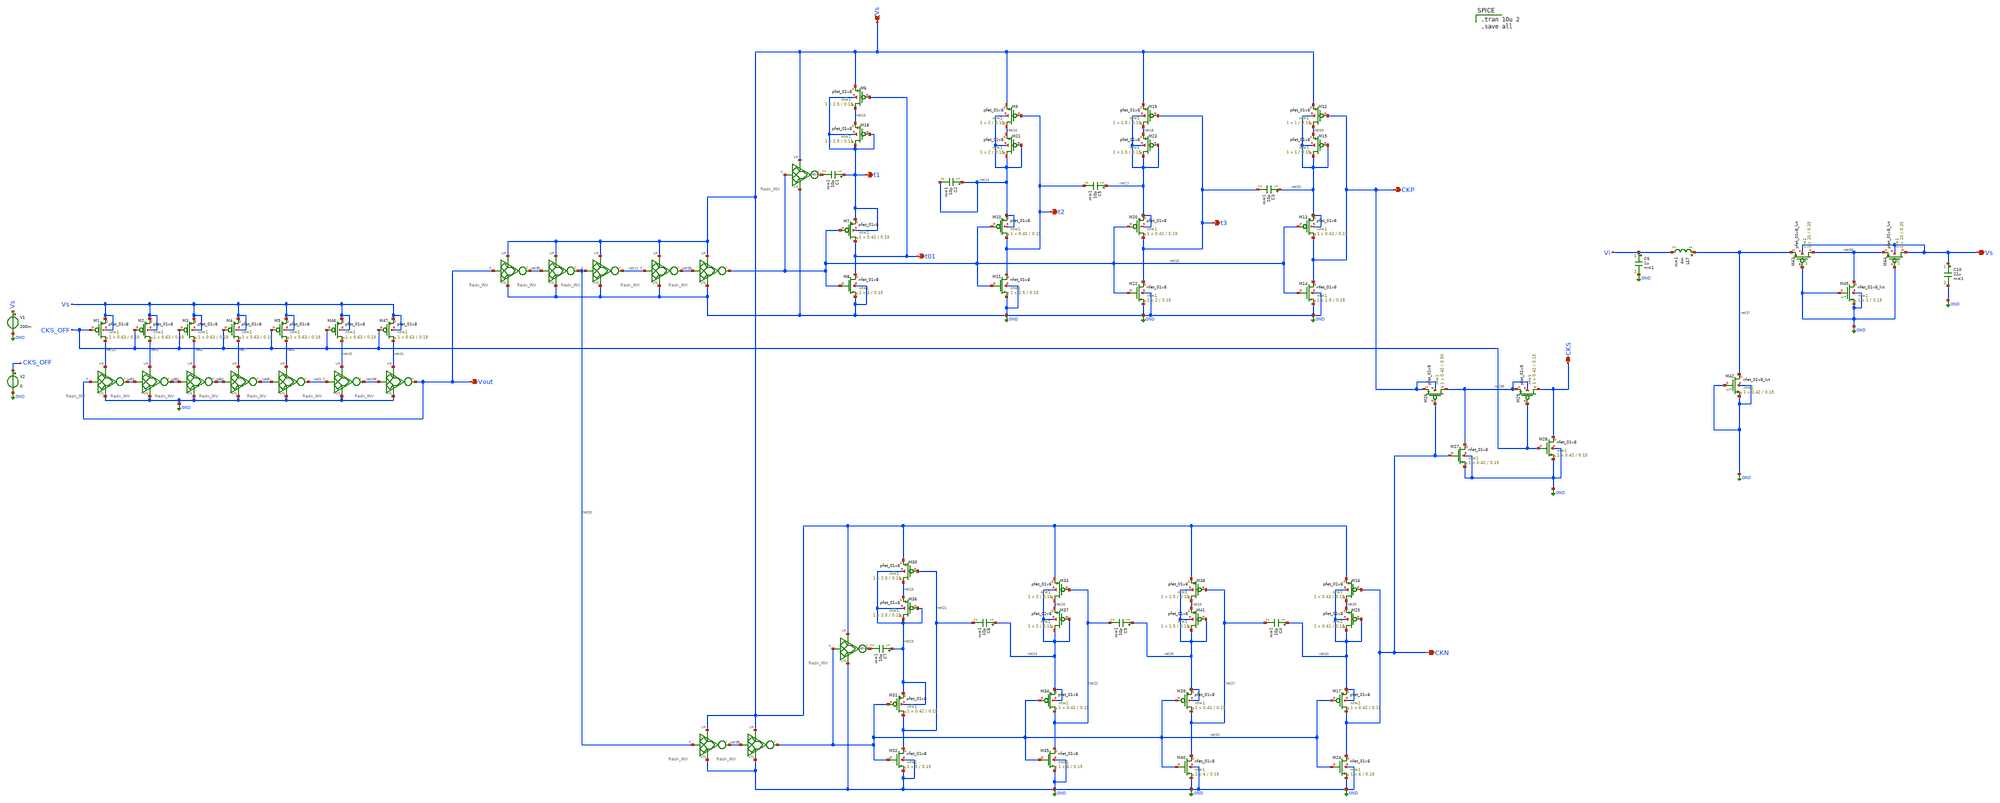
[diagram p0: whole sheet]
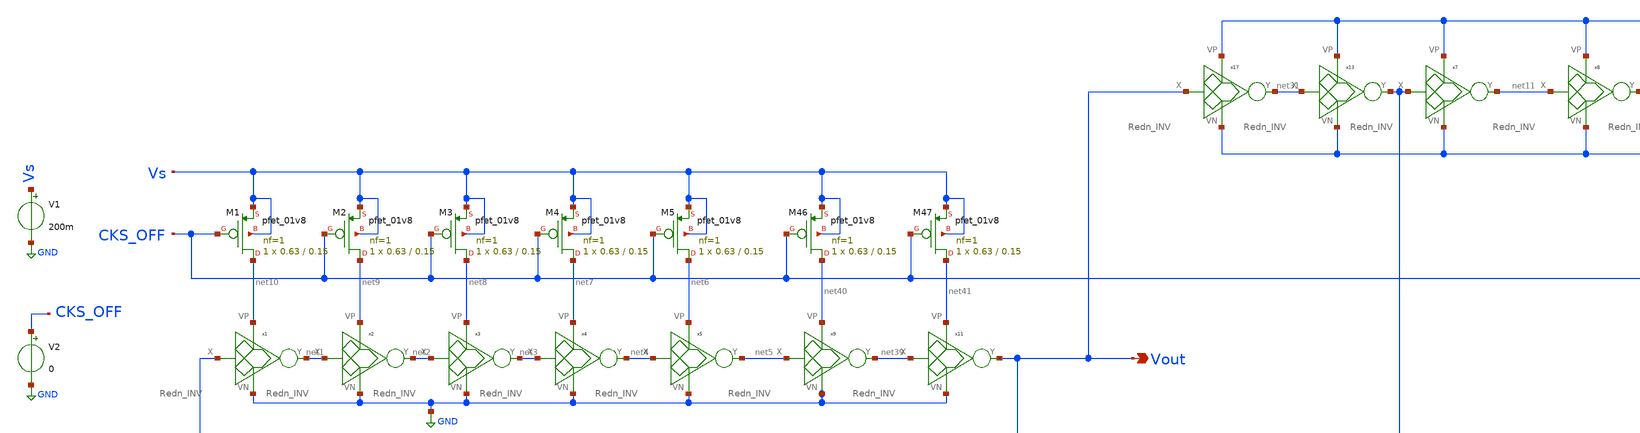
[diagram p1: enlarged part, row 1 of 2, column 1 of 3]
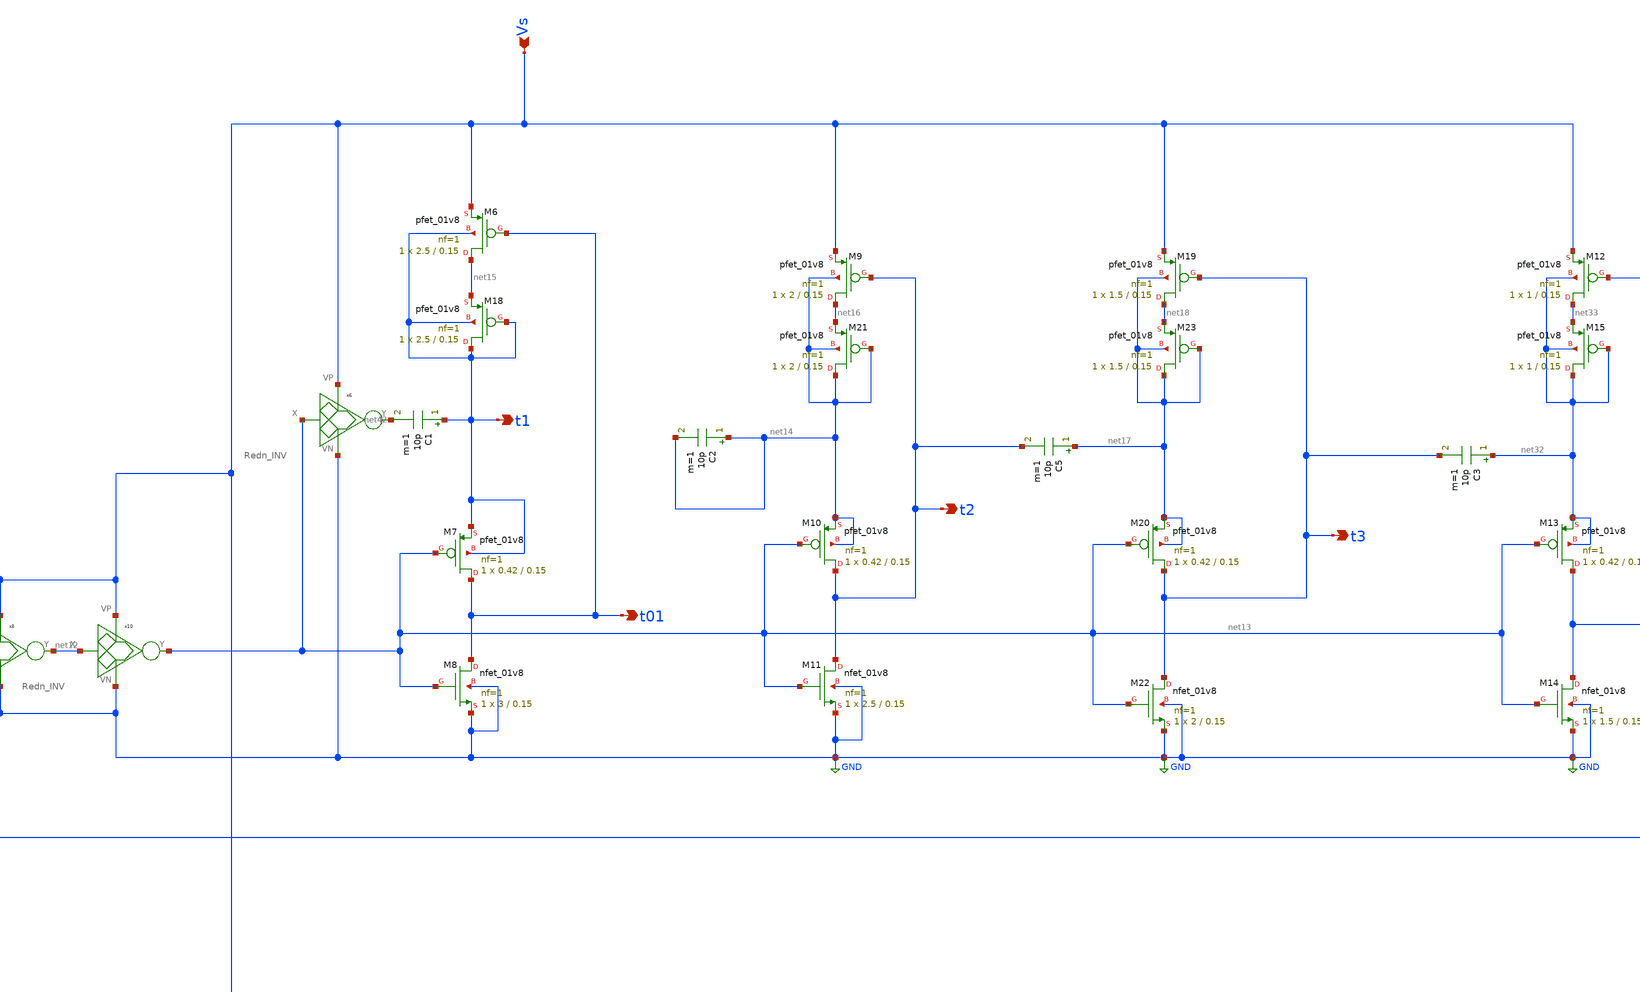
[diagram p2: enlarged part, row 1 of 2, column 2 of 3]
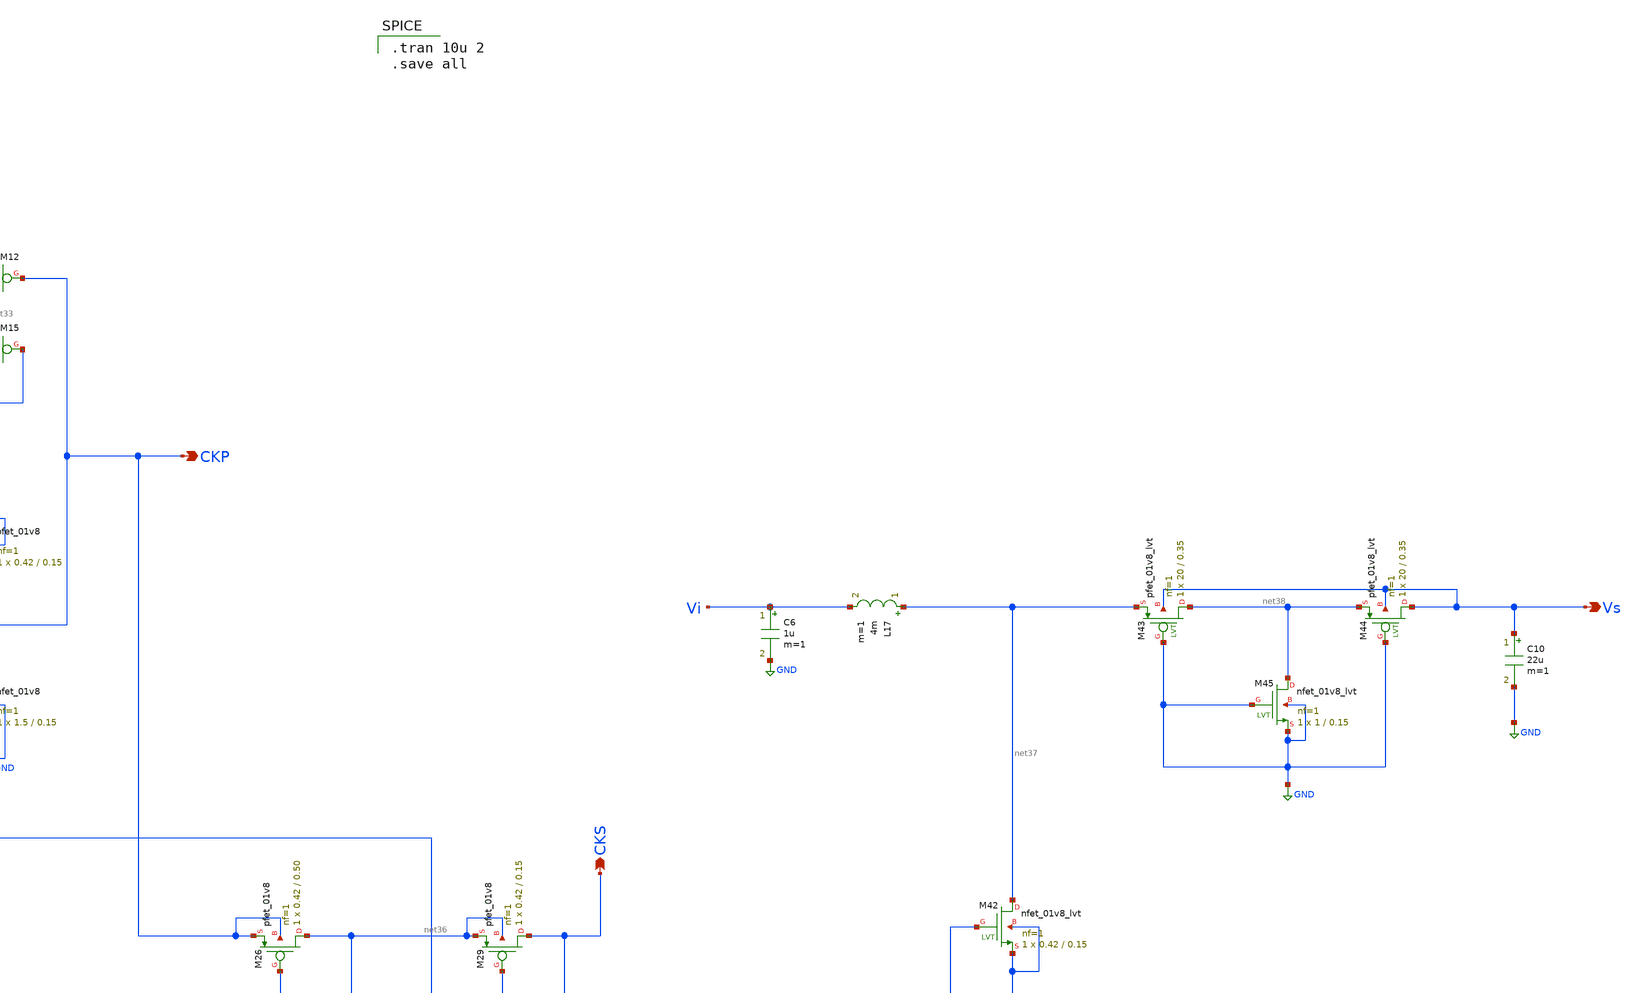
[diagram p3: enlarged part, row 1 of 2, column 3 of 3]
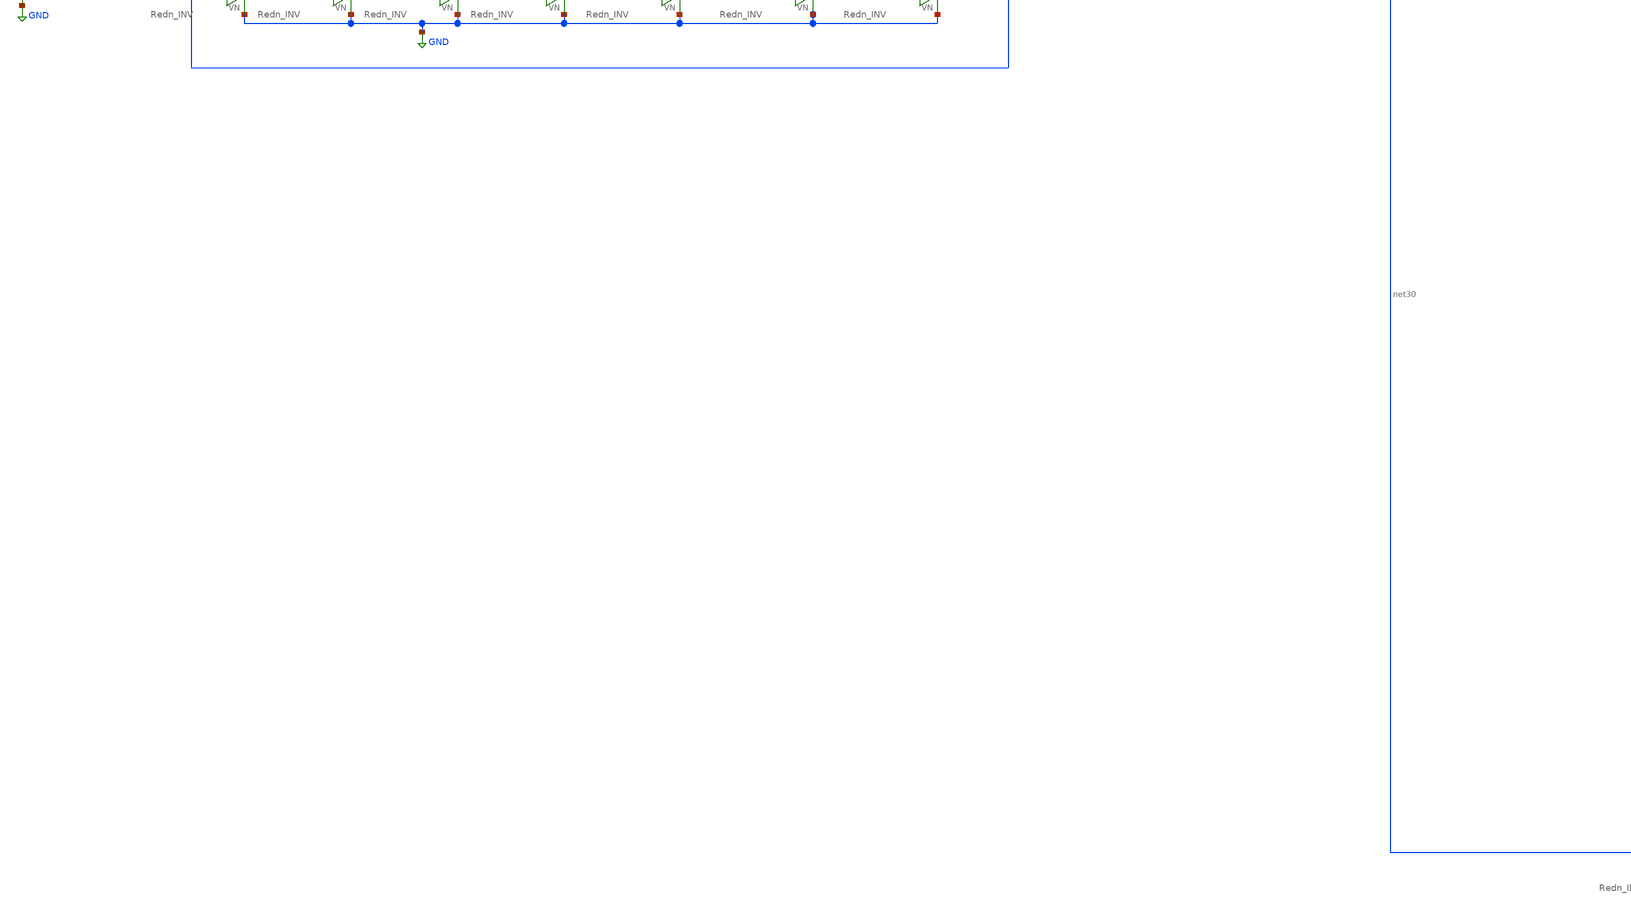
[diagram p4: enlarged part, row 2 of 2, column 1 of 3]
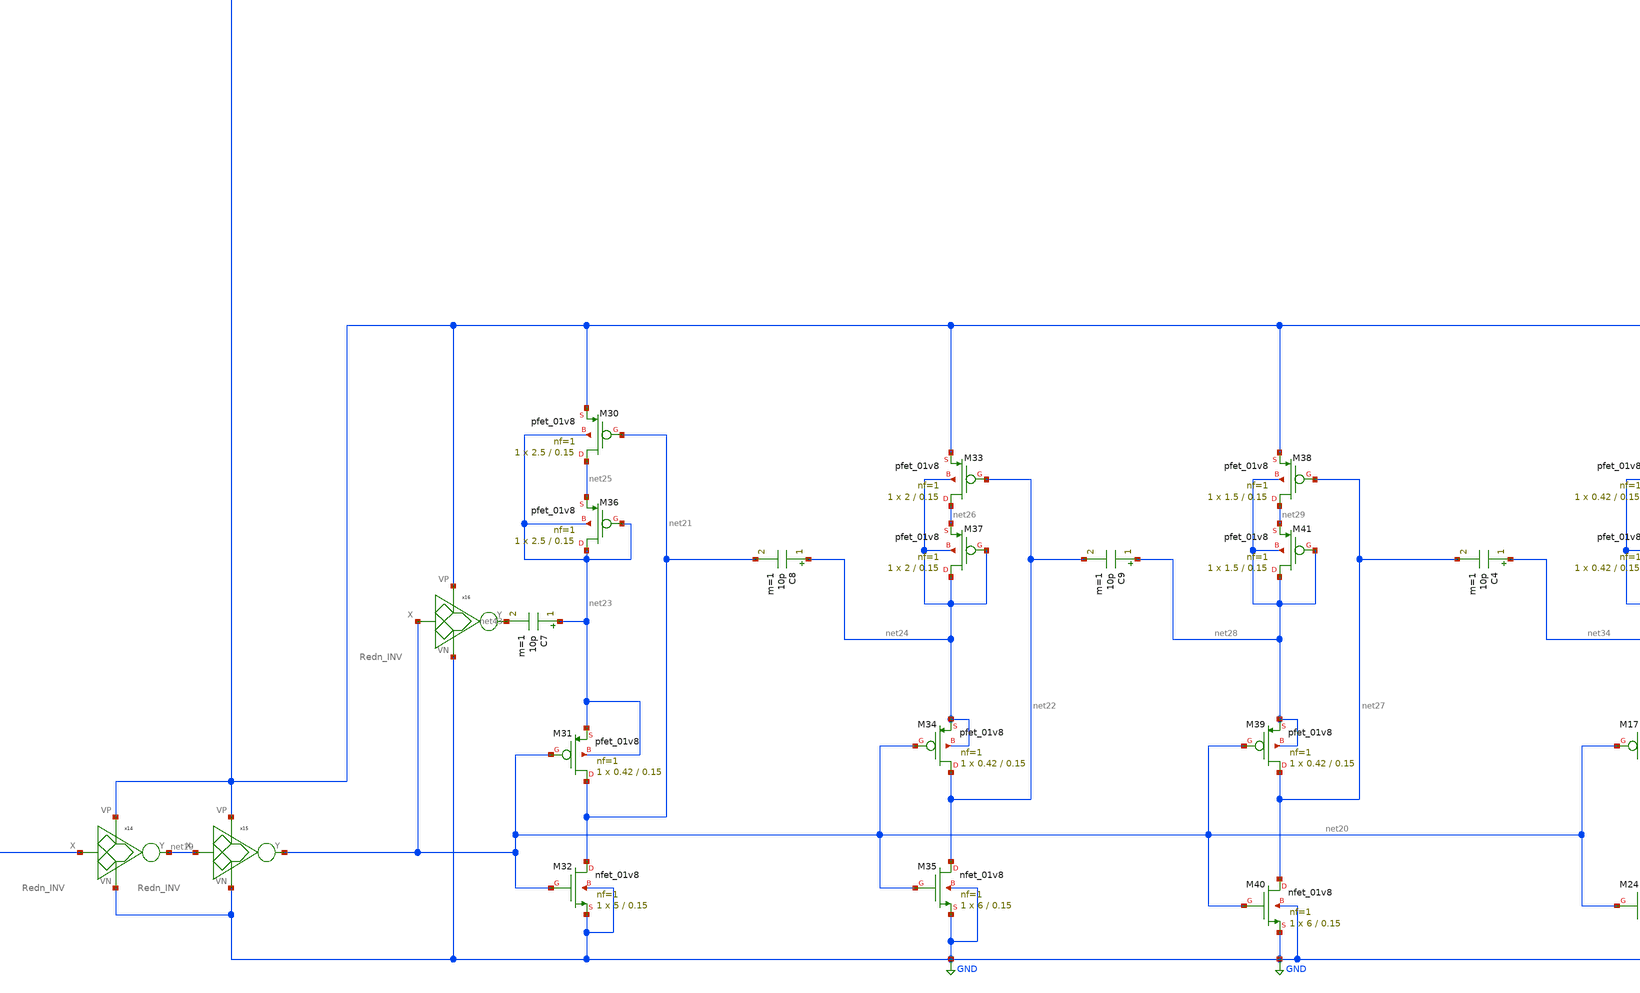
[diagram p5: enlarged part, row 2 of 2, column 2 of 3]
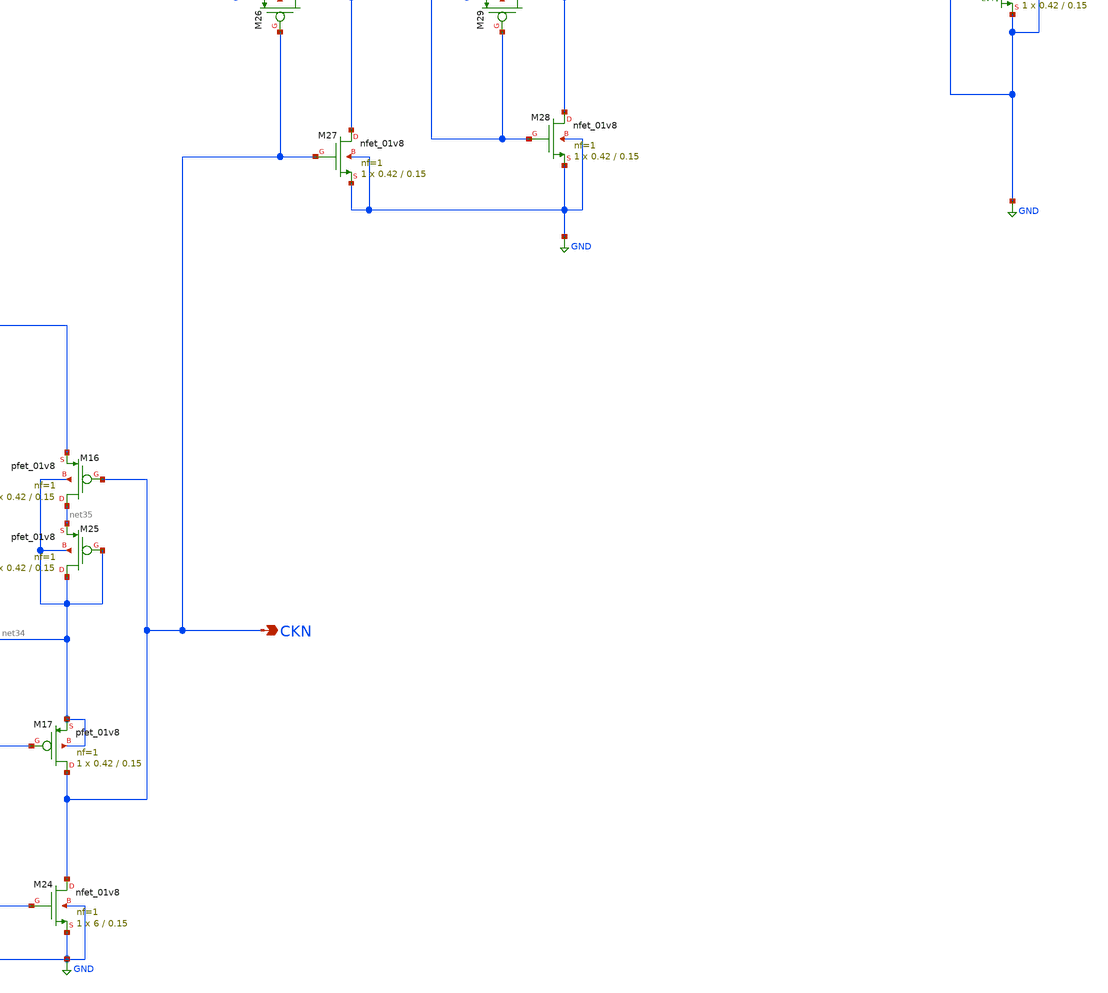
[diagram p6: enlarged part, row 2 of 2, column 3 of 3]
** sch_path: Blocks/Startup Converter/test_2.sch
**.subckt test_2 Vout Vs t1 t2 CKP CKN CKS Vs t3 t01
*.opin Vout
*.ipin Vs
*.opin t1
*.opin t2
*.opin CKP
*.opin CKN
*.opin CKS
*.opin Vs
*.opin t3
*.opin t01
V1 Vs GND 200m
XM1 net10 CKS_OFF Vs Vs sky130_fd_pr__pfet_01v8 L=0.15 W=0.63 nf=1 ad='int((nf+1)/2) * W/nf * 0.29' as='int((nf+2)/2) * W/nf * 0.29'
+ pd='2*int((nf+1)/2) * (W/nf + 0.29)' ps='2*int((nf+2)/2) * (W/nf + 0.29)' nrd='0.29 / W' nrs='0.29 / W'
+ sa=0 sb=0 sd=0 mult=1 m=1
XM2 net9 CKS_OFF Vs Vs sky130_fd_pr__pfet_01v8 L=0.15 W=0.63 nf=1 ad='int((nf+1)/2) * W/nf * 0.29' as='int((nf+2)/2) * W/nf * 0.29'
+ pd='2*int((nf+1)/2) * (W/nf + 0.29)' ps='2*int((nf+2)/2) * (W/nf + 0.29)' nrd='0.29 / W' nrs='0.29 / W'
+ sa=0 sb=0 sd=0 mult=1 m=1
XM3 net8 CKS_OFF Vs Vs sky130_fd_pr__pfet_01v8 L=0.15 W=0.63 nf=1 ad='int((nf+1)/2) * W/nf * 0.29' as='int((nf+2)/2) * W/nf * 0.29'
+ pd='2*int((nf+1)/2) * (W/nf + 0.29)' ps='2*int((nf+2)/2) * (W/nf + 0.29)' nrd='0.29 / W' nrs='0.29 / W'
+ sa=0 sb=0 sd=0 mult=1 m=1
XM4 net7 CKS_OFF Vs Vs sky130_fd_pr__pfet_01v8 L=0.15 W=0.63 nf=1 ad='int((nf+1)/2) * W/nf * 0.29' as='int((nf+2)/2) * W/nf * 0.29'
+ pd='2*int((nf+1)/2) * (W/nf + 0.29)' ps='2*int((nf+2)/2) * (W/nf + 0.29)' nrd='0.29 / W' nrs='0.29 / W'
+ sa=0 sb=0 sd=0 mult=1 m=1
XM5 net6 CKS_OFF Vs Vs sky130_fd_pr__pfet_01v8 L=0.15 W=0.63 nf=1 ad='int((nf+1)/2) * W/nf * 0.29' as='int((nf+2)/2) * W/nf * 0.29'
+ pd='2*int((nf+1)/2) * (W/nf + 0.29)' ps='2*int((nf+2)/2) * (W/nf + 0.29)' nrd='0.29 / W' nrs='0.29 / W'
+ sa=0 sb=0 sd=0 mult=1 m=1
V2 CKS_OFF GND 0
x1 Vout net1 net10 GND Redn_INV
x2 net1 net2 net9 GND Redn_INV
x3 net2 net3 net8 GND Redn_INV
x4 net3 net4 net7 GND Redn_INV
x5 net4 net5 net6 GND Redn_INV
C1 t1 net42 10p m=1
XM6 net15 t01 Vs t1 sky130_fd_pr__pfet_01v8 L=0.15 W=2.5 nf=1 ad='int((nf+1)/2) * W/nf * 0.29' as='int((nf+2)/2) * W/nf * 0.29'
+ pd='2*int((nf+1)/2) * (W/nf + 0.29)' ps='2*int((nf+2)/2) * (W/nf + 0.29)' nrd='0.29 / W' nrs='0.29 / W'
+ sa=0 sb=0 sd=0 mult=1 m=1
XM7 t01 net13 t1 t1 sky130_fd_pr__pfet_01v8 L=0.15 W=0.42 nf=1 ad='int((nf+1)/2) * W/nf * 0.29' as='int((nf+2)/2) * W/nf * 0.29'
+ pd='2*int((nf+1)/2) * (W/nf + 0.29)' ps='2*int((nf+2)/2) * (W/nf + 0.29)' nrd='0.29 / W' nrs='0.29 / W'
+ sa=0 sb=0 sd=0 mult=1 m=1
XM8 t01 net13 GND GND sky130_fd_pr__nfet_01v8 L=0.15 W=3 nf=1 ad='int((nf+1)/2) * W/nf * 0.29' as='int((nf+2)/2) * W/nf * 0.29'
+ pd='2*int((nf+1)/2) * (W/nf + 0.29)' ps='2*int((nf+2)/2) * (W/nf + 0.29)' nrd='0.29 / W' nrs='0.29 / W'
+ sa=0 sb=0 sd=0 mult=1 m=1
XM9 net16 t2 Vs net14 sky130_fd_pr__pfet_01v8 L=0.15 W=2 nf=1 ad='int((nf+1)/2) * W/nf * 0.29' as='int((nf+2)/2) * W/nf * 0.29'
+ pd='2*int((nf+1)/2) * (W/nf + 0.29)' ps='2*int((nf+2)/2) * (W/nf + 0.29)' nrd='0.29 / W' nrs='0.29 / W'
+ sa=0 sb=0 sd=0 mult=1 m=1
XM10 t2 net13 net14 net14 sky130_fd_pr__pfet_01v8 L=0.15 W=0.42 nf=1 ad='int((nf+1)/2) * W/nf * 0.29'
+ as='int((nf+2)/2) * W/nf * 0.29' pd='2*int((nf+1)/2) * (W/nf + 0.29)' ps='2*int((nf+2)/2) * (W/nf + 0.29)'
+ nrd='0.29 / W' nrs='0.29 / W' sa=0 sb=0 sd=0 mult=1 m=1
XM11 t2 net13 GND GND sky130_fd_pr__nfet_01v8 L=0.15 W=2.5 nf=1 ad='int((nf+1)/2) * W/nf * 0.29' as='int((nf+2)/2) * W/nf * 0.29'
+ pd='2*int((nf+1)/2) * (W/nf + 0.29)' ps='2*int((nf+2)/2) * (W/nf + 0.29)' nrd='0.29 / W' nrs='0.29 / W'
+ sa=0 sb=0 sd=0 mult=1 m=1
XM18 t1 t1 net15 t1 sky130_fd_pr__pfet_01v8 L=0.15 W=2.5 nf=1 ad='int((nf+1)/2) * W/nf * 0.29' as='int((nf+2)/2) * W/nf * 0.29'
+ pd='2*int((nf+1)/2) * (W/nf + 0.29)' ps='2*int((nf+2)/2) * (W/nf + 0.29)' nrd='0.29 / W' nrs='0.29 / W'
+ sa=0 sb=0 sd=0 mult=1 m=1
XM21 net14 net14 net16 net14 sky130_fd_pr__pfet_01v8 L=0.15 W=2 nf=1 ad='int((nf+1)/2) * W/nf * 0.29'
+ as='int((nf+2)/2) * W/nf * 0.29' pd='2*int((nf+1)/2) * (W/nf + 0.29)' ps='2*int((nf+2)/2) * (W/nf + 0.29)'
+ nrd='0.29 / W' nrs='0.29 / W' sa=0 sb=0 sd=0 mult=1 m=1
C2 net14 net14 10p m=1
x7 net30 net11 Vs GND Redn_INV
x8 net11 net12 Vs GND Redn_INV
x10 net12 net13 Vs GND Redn_INV
x6 net13 net42 Vs GND Redn_INV
XM19 net18 t3 Vs net17 sky130_fd_pr__pfet_01v8 L=0.15 W=1.5 nf=1 ad='int((nf+1)/2) * W/nf * 0.29' as='int((nf+2)/2) * W/nf * 0.29'
+ pd='2*int((nf+1)/2) * (W/nf + 0.29)' ps='2*int((nf+2)/2) * (W/nf + 0.29)' nrd='0.29 / W' nrs='0.29 / W'
+ sa=0 sb=0 sd=0 mult=1 m=1
XM20 t3 net13 net17 net17 sky130_fd_pr__pfet_01v8 L=0.15 W=0.42 nf=1 ad='int((nf+1)/2) * W/nf * 0.29'
+ as='int((nf+2)/2) * W/nf * 0.29' pd='2*int((nf+1)/2) * (W/nf + 0.29)' ps='2*int((nf+2)/2) * (W/nf + 0.29)'
+ nrd='0.29 / W' nrs='0.29 / W' sa=0 sb=0 sd=0 mult=1 m=1
XM22 t3 net13 GND GND sky130_fd_pr__nfet_01v8 L=0.15 W=2 nf=1 ad='int((nf+1)/2) * W/nf * 0.29' as='int((nf+2)/2) * W/nf * 0.29'
+ pd='2*int((nf+1)/2) * (W/nf + 0.29)' ps='2*int((nf+2)/2) * (W/nf + 0.29)' nrd='0.29 / W' nrs='0.29 / W'
+ sa=0 sb=0 sd=0 mult=1 m=1
XM23 net17 net17 net18 net17 sky130_fd_pr__pfet_01v8 L=0.15 W=1.5 nf=1 ad='int((nf+1)/2) * W/nf * 0.29'
+ as='int((nf+2)/2) * W/nf * 0.29' pd='2*int((nf+1)/2) * (W/nf + 0.29)' ps='2*int((nf+2)/2) * (W/nf + 0.29)'
+ nrd='0.29 / W' nrs='0.29 / W' sa=0 sb=0 sd=0 mult=1 m=1
C5 net17 t2 10p m=1
C7 net23 net43 10p m=1
XM30 net25 net21 Vs net23 sky130_fd_pr__pfet_01v8 L=0.15 W=2.5 nf=1 ad='int((nf+1)/2) * W/nf * 0.29'
+ as='int((nf+2)/2) * W/nf * 0.29' pd='2*int((nf+1)/2) * (W/nf + 0.29)' ps='2*int((nf+2)/2) * (W/nf + 0.29)'
+ nrd='0.29 / W' nrs='0.29 / W' sa=0 sb=0 sd=0 mult=1 m=1
XM31 net21 net20 net23 net23 sky130_fd_pr__pfet_01v8 L=0.15 W=0.42 nf=1 ad='int((nf+1)/2) * W/nf * 0.29'
+ as='int((nf+2)/2) * W/nf * 0.29' pd='2*int((nf+1)/2) * (W/nf + 0.29)' ps='2*int((nf+2)/2) * (W/nf + 0.29)'
+ nrd='0.29 / W' nrs='0.29 / W' sa=0 sb=0 sd=0 mult=1 m=1
XM32 net21 net20 GND GND sky130_fd_pr__nfet_01v8 L=0.15 W=5 nf=1 ad='int((nf+1)/2) * W/nf * 0.29' as='int((nf+2)/2) * W/nf * 0.29'
+ pd='2*int((nf+1)/2) * (W/nf + 0.29)' ps='2*int((nf+2)/2) * (W/nf + 0.29)' nrd='0.29 / W' nrs='0.29 / W'
+ sa=0 sb=0 sd=0 mult=1 m=1
XM33 net26 net22 Vs net24 sky130_fd_pr__pfet_01v8 L=0.15 W=2 nf=1 ad='int((nf+1)/2) * W/nf * 0.29' as='int((nf+2)/2) * W/nf * 0.29'
+ pd='2*int((nf+1)/2) * (W/nf + 0.29)' ps='2*int((nf+2)/2) * (W/nf + 0.29)' nrd='0.29 / W' nrs='0.29 / W'
+ sa=0 sb=0 sd=0 mult=1 m=1
XM34 net22 net20 net24 net24 sky130_fd_pr__pfet_01v8 L=0.15 W=0.42 nf=1 ad='int((nf+1)/2) * W/nf * 0.29'
+ as='int((nf+2)/2) * W/nf * 0.29' pd='2*int((nf+1)/2) * (W/nf + 0.29)' ps='2*int((nf+2)/2) * (W/nf + 0.29)'
+ nrd='0.29 / W' nrs='0.29 / W' sa=0 sb=0 sd=0 mult=1 m=1
XM35 net22 net20 GND GND sky130_fd_pr__nfet_01v8 L=0.15 W=6 nf=1 ad='int((nf+1)/2) * W/nf * 0.29' as='int((nf+2)/2) * W/nf * 0.29'
+ pd='2*int((nf+1)/2) * (W/nf + 0.29)' ps='2*int((nf+2)/2) * (W/nf + 0.29)' nrd='0.29 / W' nrs='0.29 / W'
+ sa=0 sb=0 sd=0 mult=1 m=1
XM36 net23 net23 net25 net23 sky130_fd_pr__pfet_01v8 L=0.15 W=2.5 nf=1 ad='int((nf+1)/2) * W/nf * 0.29'
+ as='int((nf+2)/2) * W/nf * 0.29' pd='2*int((nf+1)/2) * (W/nf + 0.29)' ps='2*int((nf+2)/2) * (W/nf + 0.29)'
+ nrd='0.29 / W' nrs='0.29 / W' sa=0 sb=0 sd=0 mult=1 m=1
XM37 net24 net24 net26 net24 sky130_fd_pr__pfet_01v8 L=0.15 W=2 nf=1 ad='int((nf+1)/2) * W/nf * 0.29'
+ as='int((nf+2)/2) * W/nf * 0.29' pd='2*int((nf+1)/2) * (W/nf + 0.29)' ps='2*int((nf+2)/2) * (W/nf + 0.29)'
+ nrd='0.29 / W' nrs='0.29 / W' sa=0 sb=0 sd=0 mult=1 m=1
C8 net24 net21 10p m=1
x14 net30 net19 Vs GND Redn_INV
x15 net19 net20 Vs GND Redn_INV
x16 net20 net43 Vs GND Redn_INV
XM38 net29 net27 Vs net28 sky130_fd_pr__pfet_01v8 L=0.15 W=1.5 nf=1 ad='int((nf+1)/2) * W/nf * 0.29'
+ as='int((nf+2)/2) * W/nf * 0.29' pd='2*int((nf+1)/2) * (W/nf + 0.29)' ps='2*int((nf+2)/2) * (W/nf + 0.29)'
+ nrd='0.29 / W' nrs='0.29 / W' sa=0 sb=0 sd=0 mult=1 m=1
XM39 net27 net20 net28 net28 sky130_fd_pr__pfet_01v8 L=0.15 W=0.42 nf=1 ad='int((nf+1)/2) * W/nf * 0.29'
+ as='int((nf+2)/2) * W/nf * 0.29' pd='2*int((nf+1)/2) * (W/nf + 0.29)' ps='2*int((nf+2)/2) * (W/nf + 0.29)'
+ nrd='0.29 / W' nrs='0.29 / W' sa=0 sb=0 sd=0 mult=1 m=1
XM40 net27 net20 GND GND sky130_fd_pr__nfet_01v8 L=0.15 W=6 nf=1 ad='int((nf+1)/2) * W/nf * 0.29' as='int((nf+2)/2) * W/nf * 0.29'
+ pd='2*int((nf+1)/2) * (W/nf + 0.29)' ps='2*int((nf+2)/2) * (W/nf + 0.29)' nrd='0.29 / W' nrs='0.29 / W'
+ sa=0 sb=0 sd=0 mult=1 m=1
XM41 net28 net28 net29 net28 sky130_fd_pr__pfet_01v8 L=0.15 W=1.5 nf=1 ad='int((nf+1)/2) * W/nf * 0.29'
+ as='int((nf+2)/2) * W/nf * 0.29' pd='2*int((nf+1)/2) * (W/nf + 0.29)' ps='2*int((nf+2)/2) * (W/nf + 0.29)'
+ nrd='0.29 / W' nrs='0.29 / W' sa=0 sb=0 sd=0 mult=1 m=1
C9 net28 net22 10p m=1
x13 net31 net30 Vs GND Redn_INV
x17 Vout net31 Vs GND Redn_INV
XM12 net33 CKP Vs net32 sky130_fd_pr__pfet_01v8 L=0.15 W=1 nf=1 ad='int((nf+1)/2) * W/nf * 0.29' as='int((nf+2)/2) * W/nf * 0.29'
+ pd='2*int((nf+1)/2) * (W/nf + 0.29)' ps='2*int((nf+2)/2) * (W/nf + 0.29)' nrd='0.29 / W' nrs='0.29 / W'
+ sa=0 sb=0 sd=0 mult=1 m=1
XM13 CKP net13 net32 net32 sky130_fd_pr__pfet_01v8 L=0.15 W=0.42 nf=1 ad='int((nf+1)/2) * W/nf * 0.29'
+ as='int((nf+2)/2) * W/nf * 0.29' pd='2*int((nf+1)/2) * (W/nf + 0.29)' ps='2*int((nf+2)/2) * (W/nf + 0.29)'
+ nrd='0.29 / W' nrs='0.29 / W' sa=0 sb=0 sd=0 mult=1 m=1
XM14 CKP net13 GND GND sky130_fd_pr__nfet_01v8 L=0.15 W=1.5 nf=1 ad='int((nf+1)/2) * W/nf * 0.29' as='int((nf+2)/2) * W/nf * 0.29'
+ pd='2*int((nf+1)/2) * (W/nf + 0.29)' ps='2*int((nf+2)/2) * (W/nf + 0.29)' nrd='0.29 / W' nrs='0.29 / W'
+ sa=0 sb=0 sd=0 mult=1 m=1
XM15 net32 net32 net33 net32 sky130_fd_pr__pfet_01v8 L=0.15 W=1 nf=1 ad='int((nf+1)/2) * W/nf * 0.29'
+ as='int((nf+2)/2) * W/nf * 0.29' pd='2*int((nf+1)/2) * (W/nf + 0.29)' ps='2*int((nf+2)/2) * (W/nf + 0.29)'
+ nrd='0.29 / W' nrs='0.29 / W' sa=0 sb=0 sd=0 mult=1 m=1
C3 net32 t3 10p m=1
XM16 net35 CKN Vs net34 sky130_fd_pr__pfet_01v8 L=0.15 W=0.42 nf=1 ad='int((nf+1)/2) * W/nf * 0.29' as='int((nf+2)/2) * W/nf * 0.29'
+ pd='2*int((nf+1)/2) * (W/nf + 0.29)' ps='2*int((nf+2)/2) * (W/nf + 0.29)' nrd='0.29 / W' nrs='0.29 / W'
+ sa=0 sb=0 sd=0 mult=1 m=1
XM17 CKN net20 net34 net34 sky130_fd_pr__pfet_01v8 L=0.15 W=0.42 nf=1 ad='int((nf+1)/2) * W/nf * 0.29'
+ as='int((nf+2)/2) * W/nf * 0.29' pd='2*int((nf+1)/2) * (W/nf + 0.29)' ps='2*int((nf+2)/2) * (W/nf + 0.29)'
+ nrd='0.29 / W' nrs='0.29 / W' sa=0 sb=0 sd=0 mult=1 m=1
XM24 CKN net20 GND GND sky130_fd_pr__nfet_01v8 L=0.15 W=6 nf=1 ad='int((nf+1)/2) * W/nf * 0.29' as='int((nf+2)/2) * W/nf * 0.29'
+ pd='2*int((nf+1)/2) * (W/nf + 0.29)' ps='2*int((nf+2)/2) * (W/nf + 0.29)' nrd='0.29 / W' nrs='0.29 / W'
+ sa=0 sb=0 sd=0 mult=1 m=1
XM25 net34 net34 net35 net34 sky130_fd_pr__pfet_01v8 L=0.15 W=0.42 nf=1 ad='int((nf+1)/2) * W/nf * 0.29'
+ as='int((nf+2)/2) * W/nf * 0.29' pd='2*int((nf+1)/2) * (W/nf + 0.29)' ps='2*int((nf+2)/2) * (W/nf + 0.29)'
+ nrd='0.29 / W' nrs='0.29 / W' sa=0 sb=0 sd=0 mult=1 m=1
C4 net34 net27 10p m=1
XM26 net36 CKN CKP CKP sky130_fd_pr__pfet_01v8 L=0.50 W=0.42 nf=1 ad='int((nf+1)/2) * W/nf * 0.29' as='int((nf+2)/2) * W/nf * 0.29'
+ pd='2*int((nf+1)/2) * (W/nf + 0.29)' ps='2*int((nf+2)/2) * (W/nf + 0.29)' nrd='0.29 / W' nrs='0.29 / W'
+ sa=0 sb=0 sd=0 mult=1 m=1
XM27 net36 CKN GND GND sky130_fd_pr__nfet_01v8 L=0.15 W=0.42 nf=1 ad='int((nf+1)/2) * W/nf * 0.29' as='int((nf+2)/2) * W/nf * 0.29'
+ pd='2*int((nf+1)/2) * (W/nf + 0.29)' ps='2*int((nf+2)/2) * (W/nf + 0.29)' nrd='0.29 / W' nrs='0.29 / W'
+ sa=0 sb=0 sd=0 mult=1 m=1
XM28 CKS CKS_OFF GND GND sky130_fd_pr__nfet_01v8 L=0.15 W=0.42 nf=1 ad='int((nf+1)/2) * W/nf * 0.29'
+ as='int((nf+2)/2) * W/nf * 0.29' pd='2*int((nf+1)/2) * (W/nf + 0.29)' ps='2*int((nf+2)/2) * (W/nf + 0.29)'
+ nrd='0.29 / W' nrs='0.29 / W' sa=0 sb=0 sd=0 mult=1 m=1
XM29 CKS CKS_OFF net36 net36 sky130_fd_pr__pfet_01v8 L=0.15 W=0.42 nf=1 ad='int((nf+1)/2) * W/nf * 0.29'
+ as='int((nf+2)/2) * W/nf * 0.29' pd='2*int((nf+1)/2) * (W/nf + 0.29)' ps='2*int((nf+2)/2) * (W/nf + 0.29)'
+ nrd='0.29 / W' nrs='0.29 / W' sa=0 sb=0 sd=0 mult=1 m=1
C6 Vi GND 1u m=1
L17 net37 Vi 4m m=1
C10 Vs GND 22u m=1
XM42 net37 GND GND GND sky130_fd_pr__nfet_01v8_lvt L=0.15 W=0.42 nf=1 ad='int((nf+1)/2) * W/nf * 0.29'
+ as='int((nf+2)/2) * W/nf * 0.29' pd='2*int((nf+1)/2) * (W/nf + 0.29)' ps='2*int((nf+2)/2) * (W/nf + 0.29)'
+ nrd='0.29 / W' nrs='0.29 / W' sa=0 sb=0 sd=0 mult=1 m=1
XM43 net38 GND net37 Vs sky130_fd_pr__pfet_01v8_lvt L=0.35 W=20 nf=1 ad='int((nf+1)/2) * W/nf * 0.29'
+ as='int((nf+2)/2) * W/nf * 0.29' pd='2*int((nf+1)/2) * (W/nf + 0.29)' ps='2*int((nf+2)/2) * (W/nf + 0.29)'
+ nrd='0.29 / W' nrs='0.29 / W' sa=0 sb=0 sd=0 mult=1 m=1
XM44 Vs GND net38 Vs sky130_fd_pr__pfet_01v8_lvt L=0.35 W=20 nf=1 ad='int((nf+1)/2) * W/nf * 0.29' as='int((nf+2)/2) * W/nf * 0.29'
+ pd='2*int((nf+1)/2) * (W/nf + 0.29)' ps='2*int((nf+2)/2) * (W/nf + 0.29)' nrd='0.29 / W' nrs='0.29 / W'
+ sa=0 sb=0 sd=0 mult=1 m=1
XM45 net38 GND GND GND sky130_fd_pr__nfet_01v8_lvt L=0.15 W=1 nf=1 ad='int((nf+1)/2) * W/nf * 0.29' as='int((nf+2)/2) * W/nf * 0.29'
+ pd='2*int((nf+1)/2) * (W/nf + 0.29)' ps='2*int((nf+2)/2) * (W/nf + 0.29)' nrd='0.29 / W' nrs='0.29 / W'
+ sa=0 sb=0 sd=0 mult=1 m=1
x9 net5 net39 net40 GND Redn_INV
x11 net39 Vout net41 GND Redn_INV
XM46 net40 CKS_OFF Vs Vs sky130_fd_pr__pfet_01v8 L=0.15 W=0.63 nf=1 ad='int((nf+1)/2) * W/nf * 0.29'
+ as='int((nf+2)/2) * W/nf * 0.29' pd='2*int((nf+1)/2) * (W/nf + 0.29)' ps='2*int((nf+2)/2) * (W/nf + 0.29)'
+ nrd='0.29 / W' nrs='0.29 / W' sa=0 sb=0 sd=0 mult=1 m=1
XM47 net41 CKS_OFF Vs Vs sky130_fd_pr__pfet_01v8 L=0.15 W=0.63 nf=1 ad='int((nf+1)/2) * W/nf * 0.29'
+ as='int((nf+2)/2) * W/nf * 0.29' pd='2*int((nf+1)/2) * (W/nf + 0.29)' ps='2*int((nf+2)/2) * (W/nf + 0.29)'
+ nrd='0.29 / W' nrs='0.29 / W' sa=0 sb=0 sd=0 mult=1 m=1
**** begin user architecture code

** opencircuitdesign pdks install
.lib $::SKYWATER_MODELS/sky130.lib.spice tt



.tran 10u 2
.save all

**** end user architecture code
**.ends

* expanding   symbol:  component/Reduntant_Inverter/Redn_INV.sym # of pins=4
** sym_path: component/Reduntant_Inverter/Redn_INV.sym
** sch_path: component/Reduntant_Inverter/Redn_INV.sch
.subckt Redn_INV X Y VP VN
*.opin Y
*.ipin X
*.iopin VP
*.iopin VN
XM15 net4 X VN VN sky130_fd_pr__nfet_01v8_lvt L=0.15 W=1 nf=1 ad='int((nf+1)/2) * W/nf * 0.29' as='int((nf+2)/2) * W/nf * 0.29'
+ pd='2*int((nf+1)/2) * (W/nf + 0.29)' ps='2*int((nf+2)/2) * (W/nf + 0.29)' nrd='0.29 / W' nrs='0.29 / W'
+ sa=0 sb=0 sd=0 mult=1 m=1
XM1 net5 X net3 VN sky130_fd_pr__nfet_01v8_lvt L=0.15 W=3.25 nf=1 ad='int((nf+1)/2) * W/nf * 0.29' as='int((nf+2)/2) * W/nf * 0.29'
+ pd='2*int((nf+1)/2) * (W/nf + 0.29)' ps='2*int((nf+2)/2) * (W/nf + 0.29)' nrd='0.29 / W' nrs='0.29 / W'
+ sa=0 sb=0 sd=0 mult=1 m=1
XM16 Y X net6 VN sky130_fd_pr__nfet_01v8_lvt L=0.15 W=6.5 nf=1 ad='int((nf+1)/2) * W/nf * 0.29' as='int((nf+2)/2) * W/nf * 0.29'
+ pd='2*int((nf+1)/2) * (W/nf + 0.29)' ps='2*int((nf+2)/2) * (W/nf + 0.29)' nrd='0.29 / W' nrs='0.29 / W'
+ sa=0 sb=0 sd=0 mult=1 m=1
XM17 net3 X VN VN sky130_fd_pr__nfet_01v8_lvt L=0.15 W=3.25 nf=1 ad='int((nf+1)/2) * W/nf * 0.29' as='int((nf+2)/2) * W/nf * 0.29'
+ pd='2*int((nf+1)/2) * (W/nf + 0.29)' ps='2*int((nf+2)/2) * (W/nf + 0.29)' nrd='0.29 / W' nrs='0.29 / W'
+ sa=0 sb=0 sd=0 mult=1 m=1
XM18 net2 X VN VN sky130_fd_pr__nfet_01v8_lvt L=0.15 W=1.5 nf=1 ad='int((nf+1)/2) * W/nf * 0.29' as='int((nf+2)/2) * W/nf * 0.29'
+ pd='2*int((nf+1)/2) * (W/nf + 0.29)' ps='2*int((nf+2)/2) * (W/nf + 0.29)' nrd='0.29 / W' nrs='0.29 / W'
+ sa=0 sb=0 sd=0 mult=1 m=1
XM19 net1 X VN VN sky130_fd_pr__nfet_01v8_lvt L=0.15 W=6.5 nf=1 ad='int((nf+1)/2) * W/nf * 0.29' as='int((nf+2)/2) * W/nf * 0.29'
+ pd='2*int((nf+1)/2) * (W/nf + 0.29)' ps='2*int((nf+2)/2) * (W/nf + 0.29)' nrd='0.29 / W' nrs='0.29 / W'
+ sa=0 sb=0 sd=0 mult=1 m=1
XM20 net6 X net1 VN sky130_fd_pr__nfet_01v8_lvt L=0.15 W=6.5 nf=1 ad='int((nf+1)/2) * W/nf * 0.29' as='int((nf+2)/2) * W/nf * 0.29'
+ pd='2*int((nf+1)/2) * (W/nf + 0.29)' ps='2*int((nf+2)/2) * (W/nf + 0.29)' nrd='0.29 / W' nrs='0.29 / W'
+ sa=0 sb=0 sd=0 mult=1 m=1
XM2 net4 X VP VP sky130_fd_pr__pfet_01v8 L=0.15 W=10 nf=1 ad='int((nf+1)/2) * W/nf * 0.29' as='int((nf+2)/2) * W/nf * 0.29'
+ pd='2*int((nf+1)/2) * (W/nf + 0.29)' ps='2*int((nf+2)/2) * (W/nf + 0.29)' nrd='0.29 / W' nrs='0.29 / W'
+ sa=0 sb=0 sd=0 mult=1 m=1
XM5 net5 X net4 net4 sky130_fd_pr__pfet_01v8 L=0.15 W=10 nf=1 ad='int((nf+1)/2) * W/nf * 0.29' as='int((nf+2)/2) * W/nf * 0.29'
+ pd='2*int((nf+1)/2) * (W/nf + 0.29)' ps='2*int((nf+2)/2) * (W/nf + 0.29)' nrd='0.29 / W' nrs='0.29 / W'
+ sa=0 sb=0 sd=0 mult=1 m=1
XM6 Y X net5 VP sky130_fd_pr__pfet_01v8 L=0.15 W=10 nf=1 ad='int((nf+1)/2) * W/nf * 0.29' as='int((nf+2)/2) * W/nf * 0.29'
+ pd='2*int((nf+1)/2) * (W/nf + 0.29)' ps='2*int((nf+2)/2) * (W/nf + 0.29)' nrd='0.29 / W' nrs='0.29 / W'
+ sa=0 sb=0 sd=0 mult=1 m=1
XM8 net3 X VP VP sky130_fd_pr__pfet_01v8 L=0.15 W=2 nf=1 ad='int((nf+1)/2) * W/nf * 0.29' as='int((nf+2)/2) * W/nf * 0.29'
+ pd='2*int((nf+1)/2) * (W/nf + 0.29)' ps='2*int((nf+2)/2) * (W/nf + 0.29)' nrd='0.29 / W' nrs='0.29 / W'
+ sa=0 sb=0 sd=0 mult=1 m=1
XM12 net2 X VP VP sky130_fd_pr__pfet_01v8 L=0.15 W=5 nf=1 ad='int((nf+1)/2) * W/nf * 0.29' as='int((nf+2)/2) * W/nf * 0.29'
+ pd='2*int((nf+1)/2) * (W/nf + 0.29)' ps='2*int((nf+2)/2) * (W/nf + 0.29)' nrd='0.29 / W' nrs='0.29 / W'
+ sa=0 sb=0 sd=0 mult=1 m=1
XM14 net6 X net2 VP sky130_fd_pr__pfet_01v8 L=0.15 W=5 nf=1 ad='int((nf+1)/2) * W/nf * 0.29' as='int((nf+2)/2) * W/nf * 0.29'
+ pd='2*int((nf+1)/2) * (W/nf + 0.29)' ps='2*int((nf+2)/2) * (W/nf + 0.29)' nrd='0.29 / W' nrs='0.29 / W'
+ sa=0 sb=0 sd=0 mult=1 m=1
XM21 net1 X VP VP sky130_fd_pr__pfet_01v8 L=0.15 W=1.5 nf=1 ad='int((nf+1)/2) * W/nf * 0.29' as='int((nf+2)/2) * W/nf * 0.29'
+ pd='2*int((nf+1)/2) * (W/nf + 0.29)' ps='2*int((nf+2)/2) * (W/nf + 0.29)' nrd='0.29 / W' nrs='0.29 / W'
+ sa=0 sb=0 sd=0 mult=1 m=1
.ends

.GLOBAL GND
.end
